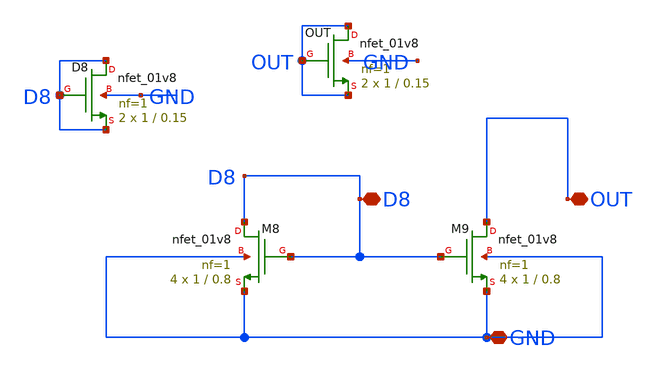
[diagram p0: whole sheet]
** sch_path: opamp/mag/nmos89/nmos89.sch
**.subckt nmos89 GND OUT D8
*.iopin GND
*.iopin OUT
*.iopin D8
XM8 D8 D8 GND GND sky130_fd_pr__nfet_01v8 L=0.8 W=1 nf=1 ad='int((nf+1)/2) * W/nf * 0.29' as='int((nf+2)/2) * W/nf * 0.29'
+ pd='2*int((nf+1)/2) * (W/nf + 0.29)' ps='2*int((nf+2)/2) * (W/nf + 0.29)' nrd='0.29 / W' nrs='0.29 / W'
+ sa=0 sb=0 sd=0 mult=4 m=4
XM9 OUT D8 GND GND sky130_fd_pr__nfet_01v8 L=0.8 W=1 nf=1 ad='int((nf+1)/2) * W/nf * 0.29' as='int((nf+2)/2) * W/nf * 0.29'
+ pd='2*int((nf+1)/2) * (W/nf + 0.29)' ps='2*int((nf+2)/2) * (W/nf + 0.29)' nrd='0.29 / W' nrs='0.29 / W'
+ sa=0 sb=0 sd=0 mult=4 m=4
XOUT OUT OUT OUT GND sky130_fd_pr__nfet_01v8 L=0.15 W=1 nf=1 ad='int((nf+1)/2) * W/nf * 0.29' as='int((nf+2)/2) * W/nf * 0.29'
+ pd='2*int((nf+1)/2) * (W/nf + 0.29)' ps='2*int((nf+2)/2) * (W/nf + 0.29)' nrd='0.29 / W' nrs='0.29 / W'
+ sa=0 sb=0 sd=0 mult=2 m=2
XD8 D8 D8 D8 GND sky130_fd_pr__nfet_01v8 L=0.15 W=1 nf=1 ad='int((nf+1)/2) * W/nf * 0.29' as='int((nf+2)/2) * W/nf * 0.29'
+ pd='2*int((nf+1)/2) * (W/nf + 0.29)' ps='2*int((nf+2)/2) * (W/nf + 0.29)' nrd='0.29 / W' nrs='0.29 / W'
+ sa=0 sb=0 sd=0 mult=2 m=2
**.ends
.end
